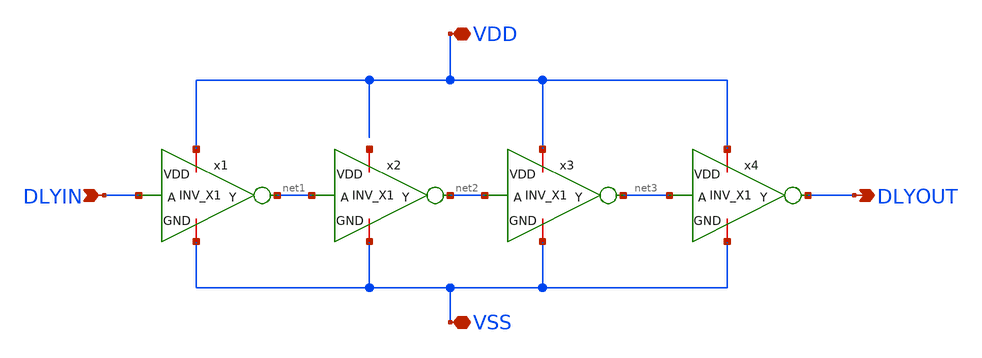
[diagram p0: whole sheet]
** sch_path: array/2word_x_2bit/DLYINV4.sch
**.subckt DLYINV4 VSS VDD DLYIN DLYOUT
*.iopin VSS
*.iopin VDD
*.ipin DLYIN
*.opin DLYOUT
x1 VDD DLYIN net1 VSS INV_X1
x2 net4 net1 net2 VSS INV_X1
x3 VDD net2 net3 VSS INV_X1
x4 VDD net3 DLYOUT VSS INV_X1
**.ends

* expanding   symbol:  TR-1um_5_stdcell/INV_X1.sym # of pins=4
** sym_path: TR-1um_5_stdcell/INV_X1.sym
** sch_path: TR-1um_5_stdcell/INV_X1.sch
.subckt INV_X1 VDD A Y GND
*.ipin A
*.opin Y
*.iopin GND
*.iopin VDD
XM7 Y A VDD VDD PMOS w=10.2u l=1u as=0 ad=0 ps=0 pd=0 nrd=0 nrs=0 m=1
XM2 Y A GND GND NMOS w=3.4u l=1u as=0 ad=0 ps=0 pd=0 nrd=0 nrs=0 m=1
.ends

.end
